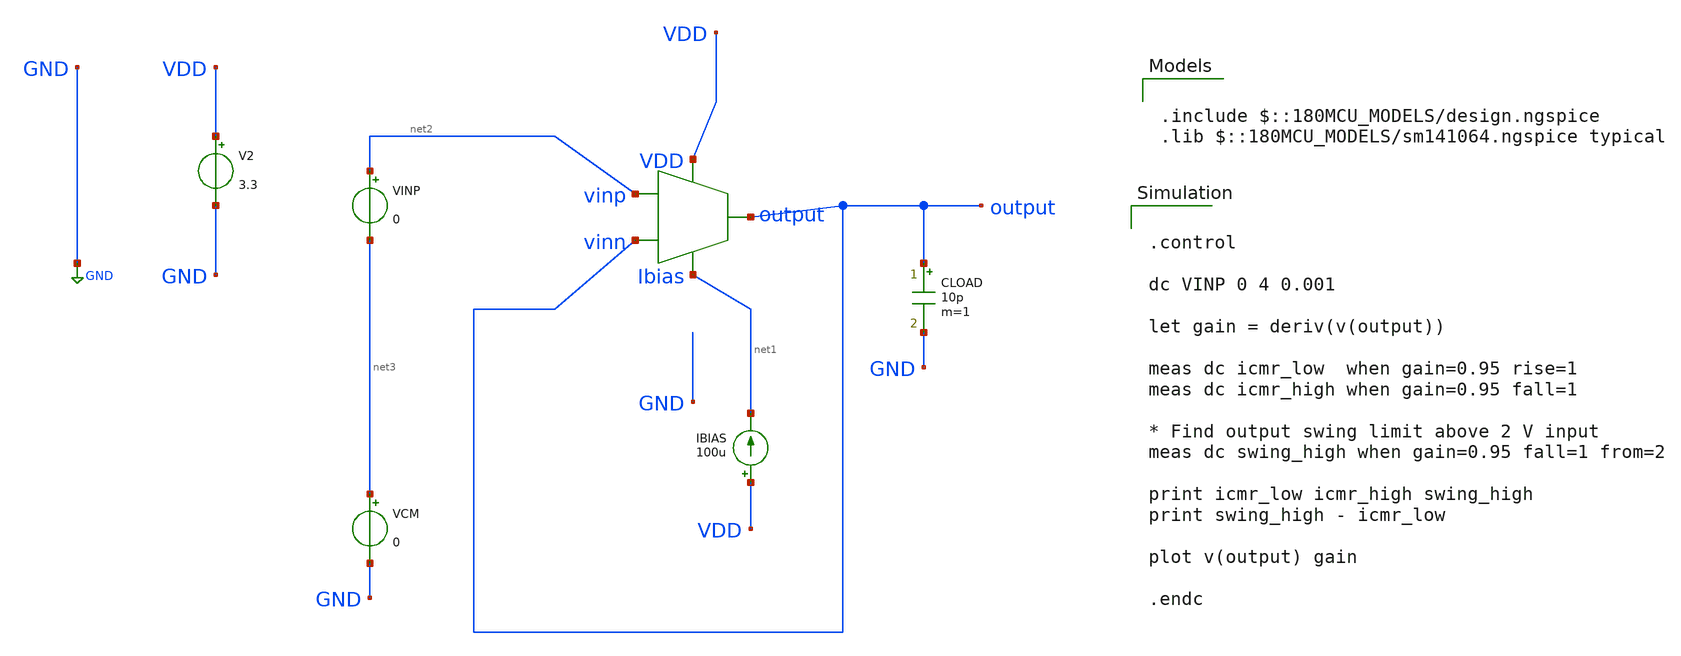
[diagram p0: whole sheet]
** sch_path: designs/libs/core_amps/ota_telescopic/telescopic_dc_unity.sch
**.subckt telescopic_dc_unity
IBIAS VDD net1 100u
V2 VDD GND 3.3
CLOAD output GND 10p m=1
VINP net2 net3 0
VCM net3 GND 0
X1 net2 output VDD net1 output telescopic_cascode
**** begin user architecture code

.include $::180MCU_MODELS/design.ngspice
.lib $::180MCU_MODELS/sm141064.ngspice typical



.control

dc VINP 0 4 0.001

let gain = deriv(v(output))

meas dc icmr_low  when gain=0.95 rise=1
meas dc icmr_high when gain=0.95 fall=1

* Find output swing limit above 2 V input
meas dc swing_high when gain=0.95 fall=1 from=2

print icmr_low icmr_high swing_high
print swing_high - icmr_low

plot v(output) gain

.endc


**** end user architecture code
**.ends

* expanding   symbol:  libs/core_amps/ota_telescopic/telescopic_cascode.sym # of pins=5
** sym_path: designs/libs/core_amps/ota_telescopic/telescopic_cascode.sym
** sch_path: designs/libs/core_amps/ota_telescopic/telescopic_cascode.sch
.subckt telescopic_cascode vinp vinn VDD Ibias output
*.ipin vinp
*.ipin vinn
*.opin output
*.iopin Ibias
*.iopin VDD
XM8 output net4 net3 VDD pfet_03v3 L=0.56u W=65u nf=1 ad='int((nf+1)/2) * W/nf * 0.18u' as='int((nf+2)/2) * W/nf * 0.18u'
+ pd='2*int((nf+1)/2) * (W/nf + 0.18u)' ps='2*int((nf+2)/2) * (W/nf + 0.18u)' nrd='0.18u / W' nrs='0.18u / W'
+ sa=0 sb=0 sd=0 m=4
XM4 output VBN1 net7 GND nfet_03v3 L=0.5u W=40u nf=1 ad='int((nf+1)/2) * W/nf * 0.18u' as='int((nf+2)/2) * W/nf * 0.18u'
+ pd='2*int((nf+1)/2) * (W/nf + 0.18u)' ps='2*int((nf+2)/2) * (W/nf + 0.18u)' nrd='0.18u / W' nrs='0.18u / W'
+ sa=0 sb=0 sd=0 m=1
XM1 net5 vinp net6 GND nfet_03v3 L=0.5u W=30u nf=1 ad='int((nf+1)/2) * W/nf * 0.18u' as='int((nf+2)/2) * W/nf * 0.18u'
+ pd='2*int((nf+1)/2) * (W/nf + 0.18u)' ps='2*int((nf+2)/2) * (W/nf + 0.18u)' nrd='0.18u / W' nrs='0.18u / W'
+ sa=0 sb=0 sd=0 m=1
XM2 net1 VBN1 net5 GND nfet_03v3 L=0.5u W=40u nf=1 ad='int((nf+1)/2) * W/nf * 0.18u' as='int((nf+2)/2) * W/nf * 0.18u'
+ pd='2*int((nf+1)/2) * (W/nf + 0.18u)' ps='2*int((nf+2)/2) * (W/nf + 0.18u)' nrd='0.18u / W' nrs='0.18u / W'
+ sa=0 sb=0 sd=0 m=1
XM3 net7 vinn net6 GND nfet_03v3 L=0.5u W=30u nf=1 ad='int((nf+1)/2) * W/nf * 0.18u' as='int((nf+2)/2) * W/nf * 0.18u'
+ pd='2*int((nf+1)/2) * (W/nf + 0.18u)' ps='2*int((nf+2)/2) * (W/nf + 0.18u)' nrd='0.18u / W' nrs='0.18u / W'
+ sa=0 sb=0 sd=0 m=1
XM5 net3 net1 VDD VDD pfet_03v3 L=0.56u W=65u nf=1 ad='int((nf+1)/2) * W/nf * 0.18u' as='int((nf+2)/2) * W/nf * 0.18u'
+ pd='2*int((nf+1)/2) * (W/nf + 0.18u)' ps='2*int((nf+2)/2) * (W/nf + 0.18u)' nrd='0.18u / W' nrs='0.18u / W'
+ sa=0 sb=0 sd=0 m=4
XM6 net1 net4 net2 VDD pfet_03v3 L=0.56u W=65u nf=1 ad='int((nf+1)/2) * W/nf * 0.18u' as='int((nf+2)/2) * W/nf * 0.18u'
+ pd='2*int((nf+1)/2) * (W/nf + 0.18u)' ps='2*int((nf+2)/2) * (W/nf + 0.18u)' nrd='0.18u / W' nrs='0.18u / W'
+ sa=0 sb=0 sd=0 m=4
XM7 net2 net1 VDD VDD pfet_03v3 L=0.56u W=65u nf=1 ad='int((nf+1)/2) * W/nf * 0.18u' as='int((nf+2)/2) * W/nf * 0.18u'
+ pd='2*int((nf+1)/2) * (W/nf + 0.18u)' ps='2*int((nf+2)/2) * (W/nf + 0.18u)' nrd='0.18u / W' nrs='0.18u / W'
+ sa=0 sb=0 sd=0 m=4
XM9 net6 Ibias GND GND nfet_03v3 L=0.28u W=15.54u nf=1 ad='int((nf+1)/2) * W/nf * 0.18u' as='int((nf+2)/2) * W/nf * 0.18u'
+ pd='2*int((nf+1)/2) * (W/nf + 0.18u)' ps='2*int((nf+2)/2) * (W/nf + 0.18u)' nrd='0.18u / W' nrs='0.18u / W'
+ sa=0 sb=0 sd=0 m=1
XM10 Ibias Ibias GND GND nfet_03v3 L=.28u W=5.18u nf=1 ad='int((nf+1)/2) * W/nf * 0.18u' as='int((nf+2)/2) * W/nf * 0.18u'
+ pd='2*int((nf+1)/2) * (W/nf + 0.18u)' ps='2*int((nf+2)/2) * (W/nf + 0.18u)' nrd='0.18u / W' nrs='0.18u / W'
+ sa=0 sb=0 sd=0 m=1
**** begin user architecture code


.include /foss/pdks/gf180mcuD/libs.tech/ngspice/design.ngspice
.lib /foss/pdks/gf180mcuD/libs.tech/ngspice/sm141064.ngspice typical

**** end user architecture code
V1 VBN1 GND 2.2
V2 net4 GND 1.6
.ends

.GLOBAL GND
.end
